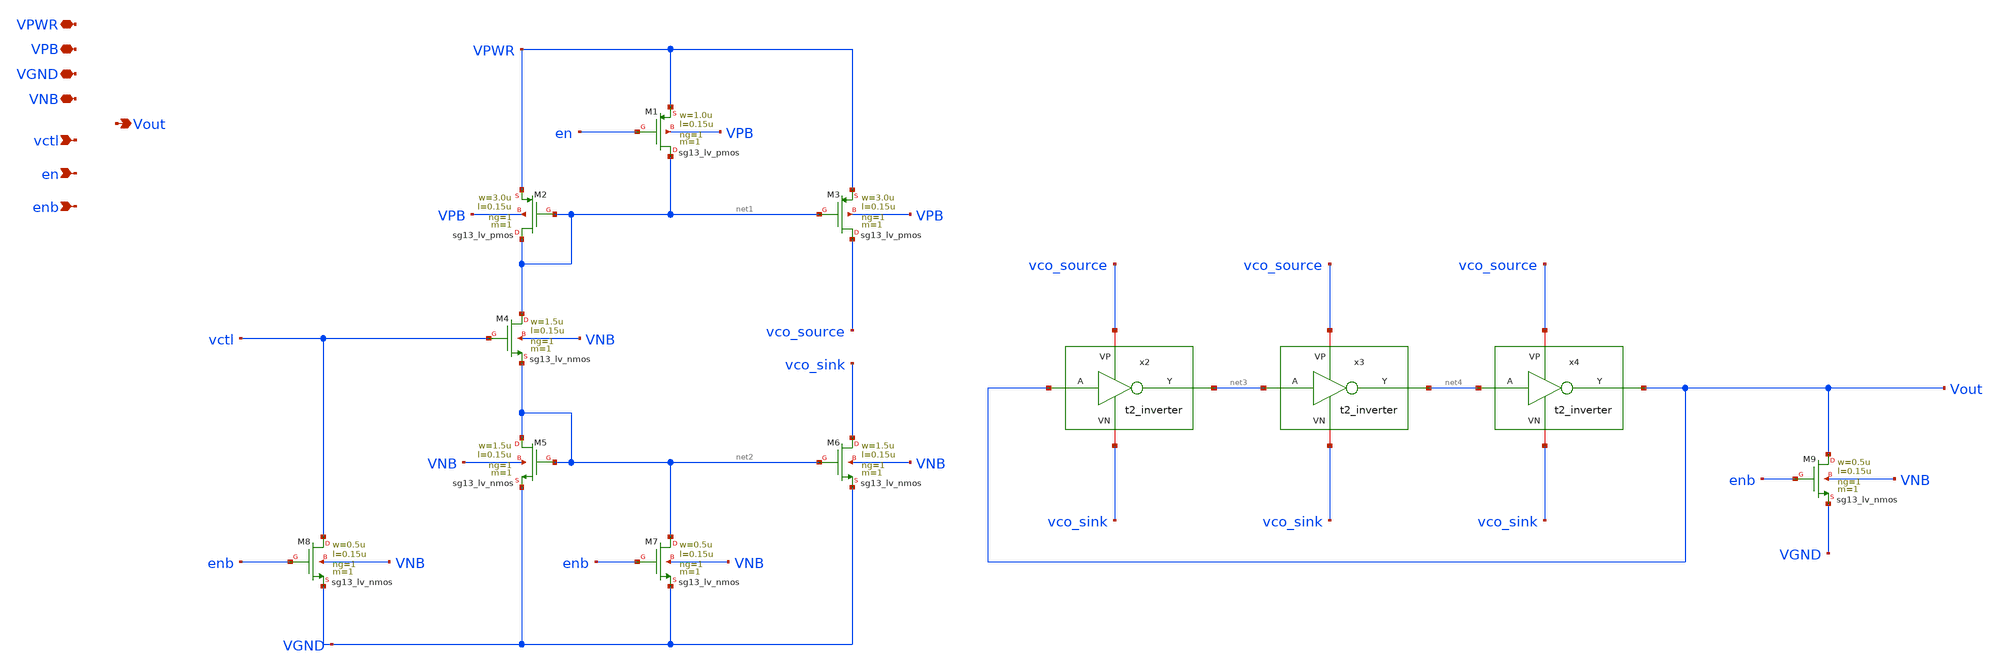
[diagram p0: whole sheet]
** sch_path: Team 2 Design/design_data/xschem/t2_vco.sch
**.subckt t2_vco VPWR VPB VGND VNB vctl en enb Vout
*.iopin VPWR
*.iopin VPB
*.iopin VGND
*.iopin VNB
*.ipin vctl
*.ipin en
*.ipin enb
*.opin Vout
XM1 net1 en VPWR VPB sg13_lv_pmos w=1.0u l=0.15u ng=1 m=1 mm_ok=1
XM2 net1 net1 VPWR VPB sg13_lv_pmos w=3.0u l=0.15u ng=1 m=1 mm_ok=1
XM3 vco_source net1 VPWR VPB sg13_lv_pmos w=3.0u l=0.15u ng=1 m=1 mm_ok=1
XM4 net1 vctl net2 VNB sg13_lv_nmos w=1.5u l=0.15u ng=1 m=1 mm_ok=1
XM5 net2 net2 VGND VNB sg13_lv_nmos w=1.5u l=0.15u ng=1 m=1 mm_ok=1
XM6 vco_sink net2 VGND VNB sg13_lv_nmos w=1.5u l=0.15u ng=1 m=1 mm_ok=1
XM7 net2 enb VGND VNB sg13_lv_nmos w=0.5u l=0.15u ng=1 m=1 mm_ok=1
XM8 vctl enb VGND VNB sg13_lv_nmos w=0.5u l=0.15u ng=1 m=1 mm_ok=1
XM9 Vout enb VGND VNB sg13_lv_nmos w=0.5u l=0.15u ng=1 m=1 mm_ok=1
x2 vco_source Vout net3 vco_sink t2_inverter
x3 vco_source net3 net4 vco_sink t2_inverter
x4 vco_source net4 Vout vco_sink t2_inverter
**.ends

* expanding   symbol:  /foss/designs/IHP/Inverter/t2_inverter.sym # of pins=4
** sym_path: Team 2 Design/design_data/xschem/t2_inverter.sym
** sch_path: Team 2 Design/design_data/xschem/t2_inverter.sch
.subckt t2_inverter VP A Y VN
*.iopin VP
*.iopin VN
*.ipin A
*.opin Y
XM2 Y A VP VP sg13_lv_pmos w=0.3u l=0.13u ng=1 m=1 mm_ok=1
XM1 Y A VN VN sg13_lv_nmos w=0.15u l=0.13u ng=1 m=1 mm_ok=1
.ends

.end
